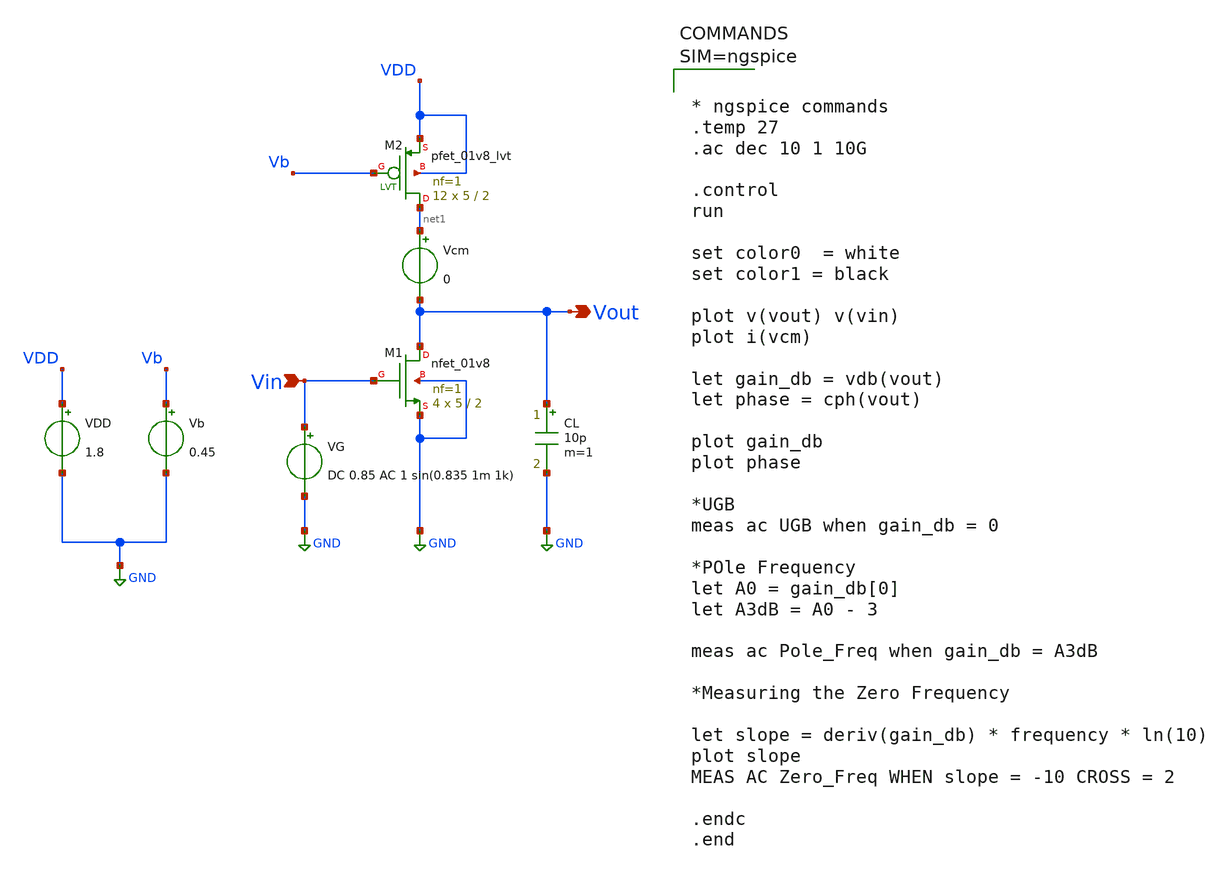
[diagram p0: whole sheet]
** sch_path: Common_Source_PMOS_Load_ckts/CS_Amp_PMOS_Triode_Load_Ckts/CS_Amp_PMOS_Triode_Load_AC_Analysis.sch
**.subckt CS_Amp_PMOS_Triode_Load_AC_Analysis Vin Vout
*.ipin Vin
*.opin Vout
XM1 Vout Vin GND GND sky130_fd_pr__nfet_01v8 L=2 W=5 nf=1 ad='int((1 + 1)/2) * 5 / 1 * 0.29' as='int((1 + 2)/2) * 5 / 1 * 0.29'
+ pd='2*int((1 + 1)/2) * (5 / 1 + 0.29)' ps='2*int((1 + 2)/2) * (5 / 1 + 0.29)' nrd='0.29 / 5 ' nrs='0.29 / 5 '
+ sa=0 sb=0 sd=0 mult=4 m=4
XM2 net1 Vb VDD VDD sky130_fd_pr__pfet_01v8_lvt L=2 W=5 nf=1 ad='int((1 + 1)/2) * 5 / 1 * 0.29' as='int((1 + 2)/2) * 5 / 1 * 0.29'
+ pd='2*int((1 + 1)/2) * (5 / 1 + 0.29)' ps='2*int((1 + 2)/2) * (5 / 1 + 0.29)' nrd='0.29 / 5 ' nrs='0.29 / 5 '
+ sa=0 sb=0 sd=0 mult=12 m=12
Vcm net1 Vout 0
VG Vin GND DC 0.85 AC 1 sin(0.835 1m 1k)
Vb Vb GND 0.45
VDD VDD GND 1.8
CL Vout GND 10p m=1
**** begin user architecture code



* ngspice commands
.temp 27
.ac dec 10 1 10G

.control
run

set color0  = white
set color1 = black

plot v(vout) v(vin)
plot i(vcm)

let gain_db = vdb(vout)
let phase = cph(vout)

plot gain_db
plot phase

*UGB
meas ac UGB when gain_db = 0

*POle Frequency
let A0 = gain_db[0]
let A3dB = A0 - 3

meas ac Pole_Freq when gain_db = A3dB

*Measuring the Zero Frequency

let slope = deriv(gain_db) * frequency * ln(10)
plot slope
MEAS AC Zero_Freq WHEN slope = -10 CROSS = 2

.endc
.end





** opencircuitdesign pdks install
.lib $::SKYWATER_MODELS/sky130.lib.spice tt

**** end user architecture code
**.ends
.GLOBAL GND
.end
